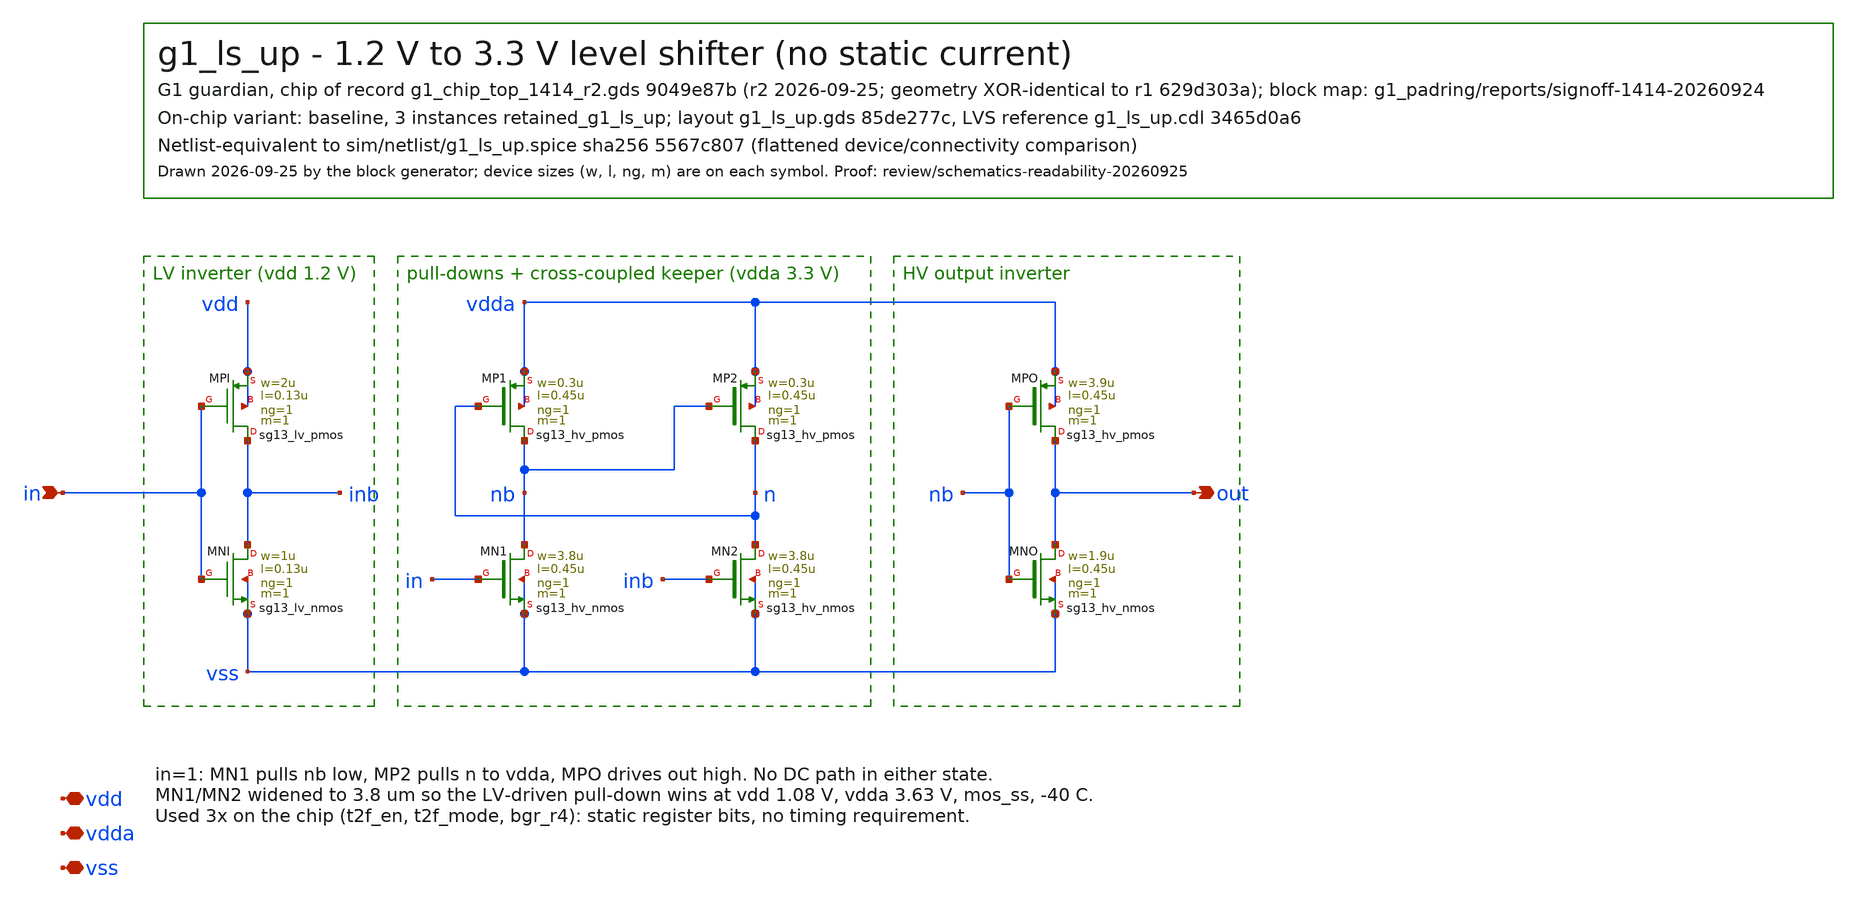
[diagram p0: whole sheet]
** sch_path: designs/g1-guardian/blocks/g1_ctrl/ls/xschem/g1_ls_up.sch
**.subckt g1_ls_up in out vdd vdda vss
*.ipin in
*.opin out
*.iopin vdd
*.iopin vdda
*.iopin vss
XMPI inb in vdd vdd sg13_lv_pmos w=2u l=0.13u ng=1 m=1 mm_ok=1
XMNI inb in vss vss sg13_lv_nmos w=1u l=0.13u ng=1 m=1 mm_ok=1
XMN1 nb in vss vss sg13_hv_nmos w=3.8u l=0.45u ng=1 m=1 mm_ok=1
XMN2 n inb vss vss sg13_hv_nmos w=3.8u l=0.45u ng=1 m=1 mm_ok=1
XMP1 nb n vdda vdda sg13_hv_pmos w=0.3u l=0.45u ng=1 m=1 mm_ok=1
XMP2 n nb vdda vdda sg13_hv_pmos w=0.3u l=0.45u ng=1 m=1 mm_ok=1
XMPO out nb vdda vdda sg13_hv_pmos w=3.9u l=0.45u ng=1 m=1 mm_ok=1
XMNO out nb vss vss sg13_hv_nmos w=1.9u l=0.45u ng=1 m=1 mm_ok=1
**.ends
.end
